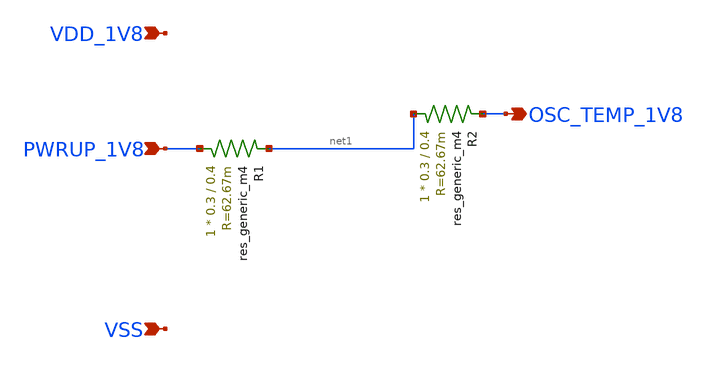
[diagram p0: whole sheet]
** sch_path: design/LELO_GR01_SKY130A/LELO_GR01.sch
**.subckt LELO_GR01 VDD_1V8 VSS PWRUP_1V8 OSC_TEMP_1V8
*.ipin VDD_1V8
*.ipin VSS
*.ipin PWRUP_1V8
*.opin OSC_TEMP_1V8
R2 net1 OSC_TEMP_1V8 sky130_fd_pr__res_generic_m4 W=0.3 L=0.4 m=1
R1 PWRUP_1V8 net1 sky130_fd_pr__res_generic_m4 W=0.3 L=0.4 m=1
**.ends
.end
